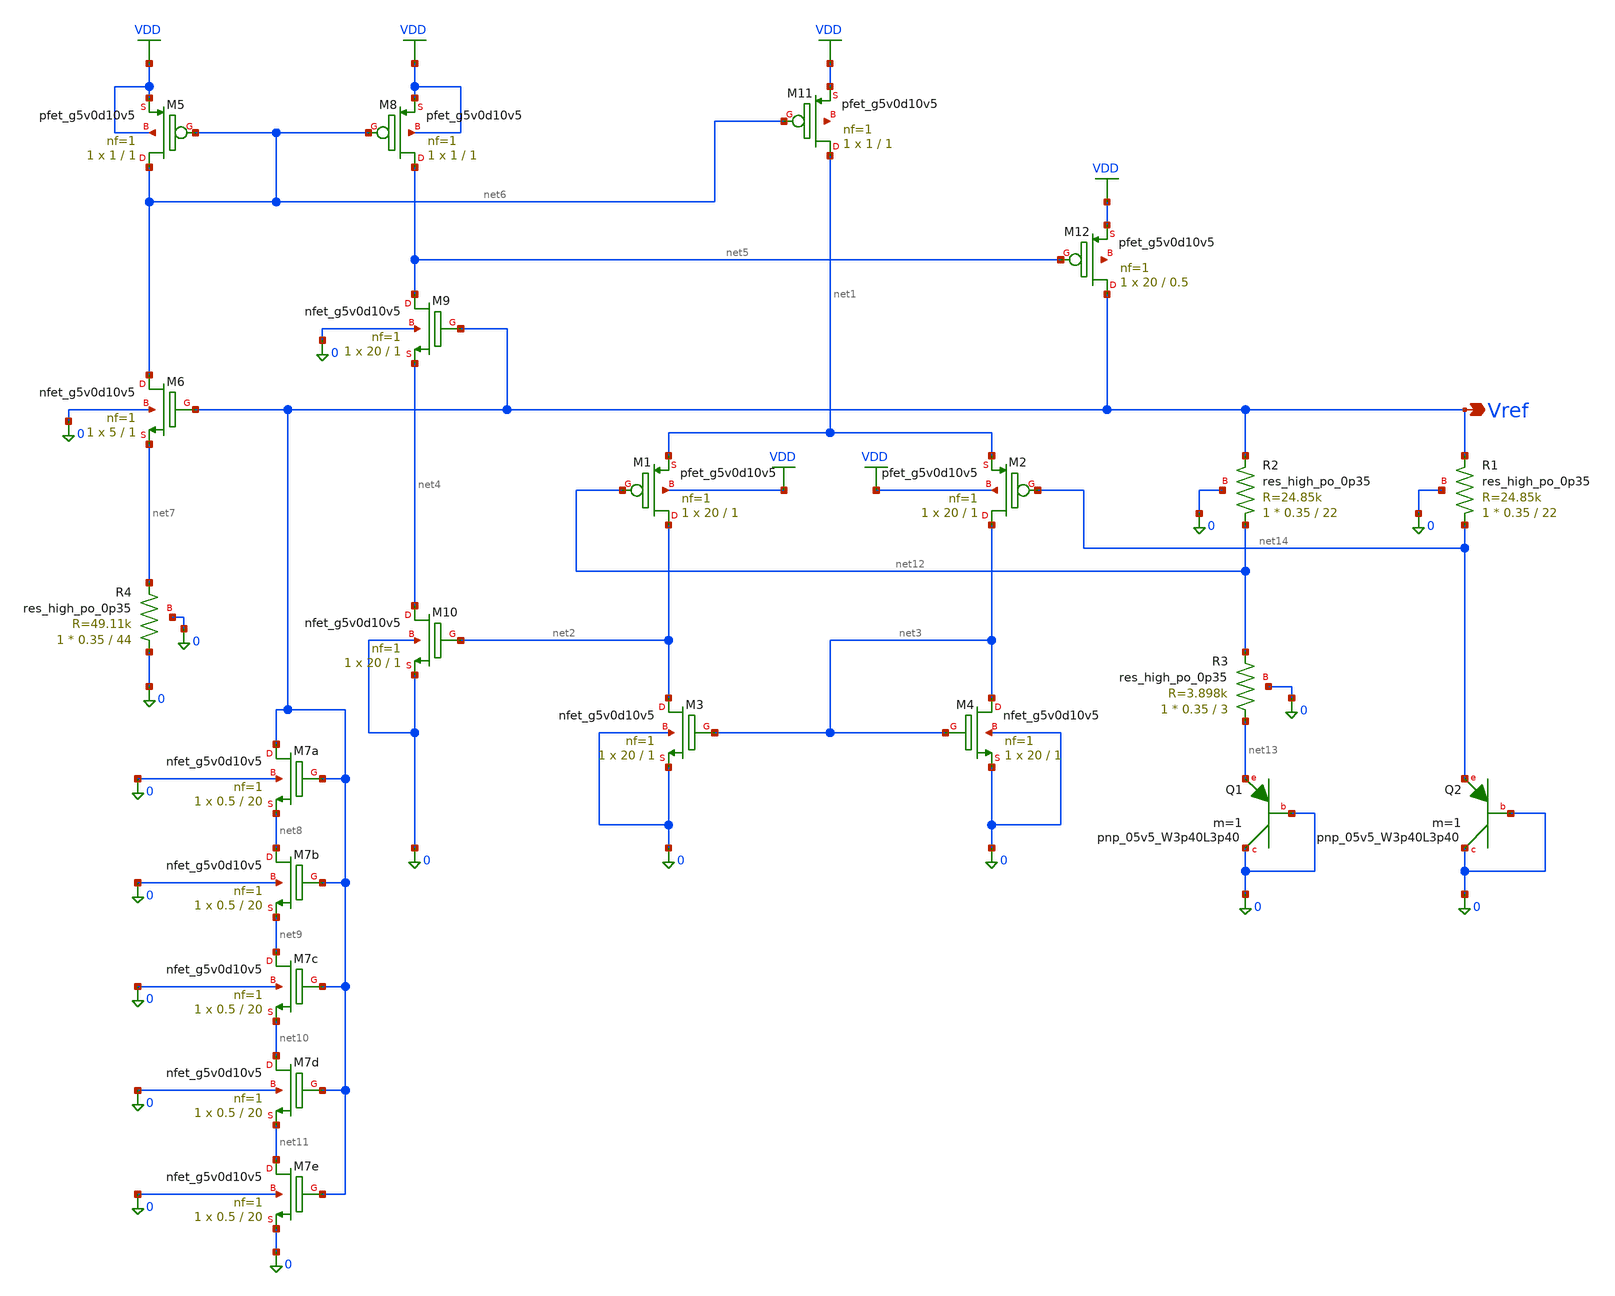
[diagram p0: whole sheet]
** sch_path: xschem/bandgap_x.sch
**.subckt bandgap_x Vref
*.opin Vref
XM2 net3 net14 net1 VDD sky130_fd_pr__pfet_g5v0d10v5 L=1 W=20 nf=1 ad='int((1 + 1)/2) * 20 / 1 * 0.29'
+ as='int((1 + 2)/2) * 20 / 1 * 0.29' pd='2*int((1 + 1)/2) * (20 / 1 + 0.29)' ps='2*int((1 + 2)/2) * (20 / 1 + 0.29)'
+ nrd='0.29 / 20 ' nrs='0.29 / 20 ' sa=0 sb=0 sd=0 mult=1 m=1
XM1 net2 net12 net1 VDD sky130_fd_pr__pfet_g5v0d10v5 L=1 W=20 nf=1 ad='int((1 + 1)/2) * 20 / 1 * 0.29'
+ as='int((1 + 2)/2) * 20 / 1 * 0.29' pd='2*int((1 + 1)/2) * (20 / 1 + 0.29)' ps='2*int((1 + 2)/2) * (20 / 1 + 0.29)'
+ nrd='0.29 / 20 ' nrs='0.29 / 20 ' sa=0 sb=0 sd=0 mult=1 m=1
XM3 net2 net3 0 0 sky130_fd_pr__nfet_g5v0d10v5 L=1 W=20 nf=1 ad='int((1 + 1)/2) * 20 / 1 * 0.29' as='int((1 + 2)/2) * 20 / 1 * 0.29'
+ pd='2*int((1 + 1)/2) * (20 / 1 + 0.29)' ps='2*int((1 + 2)/2) * (20 / 1 + 0.29)' nrd='0.29 / 20 ' nrs='0.29 / 20 '
+ sa=0 sb=0 sd=0 mult=1 m=1
XM4 net3 net3 0 0 sky130_fd_pr__nfet_g5v0d10v5 L=1 W=20 nf=1 ad='int((1 + 1)/2) * 20 / 1 * 0.29' as='int((1 + 2)/2) * 20 / 1 * 0.29'
+ pd='2*int((1 + 1)/2) * (20 / 1 + 0.29)' ps='2*int((1 + 2)/2) * (20 / 1 + 0.29)' nrd='0.29 / 20 ' nrs='0.29 / 20 '
+ sa=0 sb=0 sd=0 mult=1 m=1
XM5 net6 net6 VDD VDD sky130_fd_pr__pfet_g5v0d10v5 L=1 W=1 nf=1 ad='int((1 + 1)/2) * 1 / 1 * 0.29' as='int((1 + 2)/2) * 1 / 1 * 0.29'
+ pd='2*int((1 + 1)/2) * (1 / 1 + 0.29)' ps='2*int((1 + 2)/2) * (1 / 1 + 0.29)' nrd='0.29 / 1 ' nrs='0.29 / 1 '
+ sa=0 sb=0 sd=0 mult=1 m=1
XM6 net6 Vref net7 0 sky130_fd_pr__nfet_g5v0d10v5 L=1 W=5 nf=1 ad='int((1 + 1)/2) * 5 / 1 * 0.29' as='int((1 + 2)/2) * 5 / 1 * 0.29'
+ pd='2*int((1 + 1)/2) * (5 / 1 + 0.29)' ps='2*int((1 + 2)/2) * (5 / 1 + 0.29)' nrd='0.29 / 5 ' nrs='0.29 / 5 '
+ sa=0 sb=0 sd=0 mult=1 m=1
XM7a Vref Vref net8 0 sky130_fd_pr__nfet_g5v0d10v5 L=20 W=0.5 nf=1 ad='int((1 + 1)/2) * 0.5 / 1 * 0.29'
+ as='int((1 + 2)/2) * 0.5 / 1 * 0.29' pd='2*int((1 + 1)/2) * (0.5 / 1 + 0.29)' ps='2*int((1 + 2)/2) * (0.5 / 1 + 0.29)'
+ nrd='0.29 / 0.5 ' nrs='0.29 / 0.5 ' sa=0 sb=0 sd=0 mult=1 m=1
XM8 net5 net6 VDD VDD sky130_fd_pr__pfet_g5v0d10v5 L=1 W=1 nf=1 ad='int((1 + 1)/2) * 1 / 1 * 0.29' as='int((1 + 2)/2) * 1 / 1 * 0.29'
+ pd='2*int((1 + 1)/2) * (1 / 1 + 0.29)' ps='2*int((1 + 2)/2) * (1 / 1 + 0.29)' nrd='0.29 / 1 ' nrs='0.29 / 1 '
+ sa=0 sb=0 sd=0 mult=1 m=1
XM9 net5 Vref net4 0 sky130_fd_pr__nfet_g5v0d10v5 L=1 W=20 nf=1 ad='int((1 + 1)/2) * 20 / 1 * 0.29' as='int((1 + 2)/2) * 20 / 1 * 0.29'
+ pd='2*int((1 + 1)/2) * (20 / 1 + 0.29)' ps='2*int((1 + 2)/2) * (20 / 1 + 0.29)' nrd='0.29 / 20 ' nrs='0.29 / 20 '
+ sa=0 sb=0 sd=0 mult=1 m=1
XM10 net4 net2 0 0 sky130_fd_pr__nfet_g5v0d10v5 L=1 W=20 nf=1 ad='int((1 + 1)/2) * 20 / 1 * 0.29' as='int((1 + 2)/2) * 20 / 1 * 0.29'
+ pd='2*int((1 + 1)/2) * (20 / 1 + 0.29)' ps='2*int((1 + 2)/2) * (20 / 1 + 0.29)' nrd='0.29 / 20 ' nrs='0.29 / 20 '
+ sa=0 sb=0 sd=0 mult=1 m=1
XM11 net1 net6 VDD net15 sky130_fd_pr__pfet_g5v0d10v5 L=1 W=1 nf=1 ad='int((1 + 1)/2) * 1 / 1 * 0.29'
+ as='int((1 + 2)/2) * 1 / 1 * 0.29' pd='2*int((1 + 1)/2) * (1 / 1 + 0.29)' ps='2*int((1 + 2)/2) * (1 / 1 + 0.29)'
+ nrd='0.29 / 1 ' nrs='0.29 / 1 ' sa=0 sb=0 sd=0 mult=1 m=1
XM12 Vref net5 VDD net16 sky130_fd_pr__pfet_g5v0d10v5 L=0.5 W=20 nf=1 ad='int((1 + 1)/2) * 20 / 1 * 0.29'
+ as='int((1 + 2)/2) * 20 / 1 * 0.29' pd='2*int((1 + 1)/2) * (20 / 1 + 0.29)' ps='2*int((1 + 2)/2) * (20 / 1 + 0.29)'
+ nrd='0.29 / 20 ' nrs='0.29 / 20 ' sa=0 sb=0 sd=0 mult=1 m=1
XR1 net14 Vref 0 sky130_fd_pr__res_high_po_0p35 L=22 mult=1 m=1
XR2 net12 Vref 0 sky130_fd_pr__res_high_po_0p35 L=22 mult=1 m=1
XR3 net13 net12 0 sky130_fd_pr__res_high_po_0p35 L=3 mult=1 m=1
XR4 0 net7 0 sky130_fd_pr__res_high_po_0p35 L=44 mult=1 m=1
XQ1 0 0 net13 sky130_fd_pr__pnp_05v5_W3p40L3p40 m=1
XQ2 0 0 net14 sky130_fd_pr__pnp_05v5_W3p40L3p40 m=1
XM7b net8 Vref net9 0 sky130_fd_pr__nfet_g5v0d10v5 L=20 W=0.5 nf=1 ad='int((1 + 1)/2) * 0.5 / 1 * 0.29'
+ as='int((1 + 2)/2) * 0.5 / 1 * 0.29' pd='2*int((1 + 1)/2) * (0.5 / 1 + 0.29)' ps='2*int((1 + 2)/2) * (0.5 / 1 + 0.29)'
+ nrd='0.29 / 0.5 ' nrs='0.29 / 0.5 ' sa=0 sb=0 sd=0 mult=1 m=1
XM7c net9 Vref net10 0 sky130_fd_pr__nfet_g5v0d10v5 L=20 W=0.5 nf=1 ad='int((1 + 1)/2) * 0.5 / 1 * 0.29'
+ as='int((1 + 2)/2) * 0.5 / 1 * 0.29' pd='2*int((1 + 1)/2) * (0.5 / 1 + 0.29)' ps='2*int((1 + 2)/2) * (0.5 / 1 + 0.29)'
+ nrd='0.29 / 0.5 ' nrs='0.29 / 0.5 ' sa=0 sb=0 sd=0 mult=1 m=1
XM7d net10 Vref net11 0 sky130_fd_pr__nfet_g5v0d10v5 L=20 W=0.5 nf=1 ad='int((1 + 1)/2) * 0.5 / 1 * 0.29'
+ as='int((1 + 2)/2) * 0.5 / 1 * 0.29' pd='2*int((1 + 1)/2) * (0.5 / 1 + 0.29)' ps='2*int((1 + 2)/2) * (0.5 / 1 + 0.29)'
+ nrd='0.29 / 0.5 ' nrs='0.29 / 0.5 ' sa=0 sb=0 sd=0 mult=1 m=1
XM7e net11 Vref 0 0 sky130_fd_pr__nfet_g5v0d10v5 L=20 W=0.5 nf=1 ad='int((1 + 1)/2) * 0.5 / 1 * 0.29'
+ as='int((1 + 2)/2) * 0.5 / 1 * 0.29' pd='2*int((1 + 1)/2) * (0.5 / 1 + 0.29)' ps='2*int((1 + 2)/2) * (0.5 / 1 + 0.29)'
+ nrd='0.29 / 0.5 ' nrs='0.29 / 0.5 ' sa=0 sb=0 sd=0 mult=1 m=1
**.ends
.GLOBAL VDD
.end
